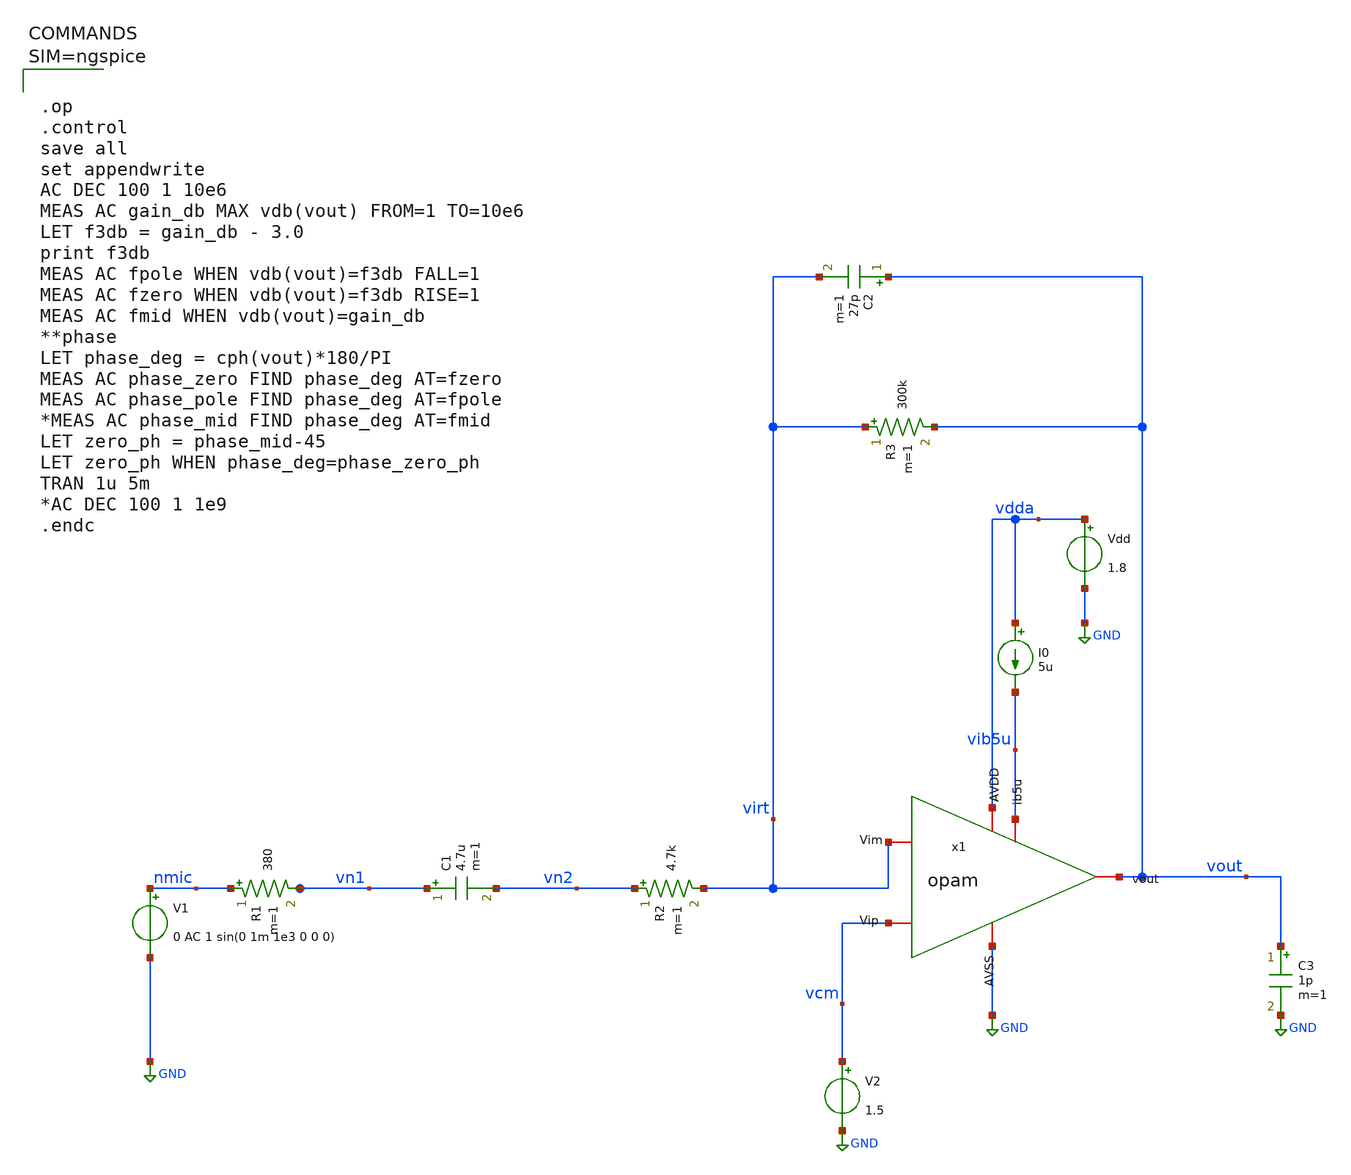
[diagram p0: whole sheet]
** sch_path: xschem/Main_opam_nmos.sch
**.subckt Main_opam_nmos
V1 nmic GND 0 AC 1 sin(0 1m 1e3 0 0 0)
R1 nmic vn1 380 m=1
C1 vn1 vn2 4.7u m=1
R2 vn2 virt 4.7k m=1
R3 virt vout 300k m=1
C2 vout virt 27p m=1
V2 vcm GND 1.5
C3 vout GND 1p m=1
x1 vdda vout virt vcm vib5u GND opam
I0 vdda vib5u 5u
Vdd vdda GND 1.8
**** begin user architecture code

** opencircuitdesign pdks install
.lib $::SKYWATER_MODELS/sky130.lib.spice tt




.op
.control
save all
set appendwrite
AC DEC 100 1 10e6
MEAS AC gain_db MAX vdb(vout) FROM=1 TO=10e6
LET f3db = gain_db - 3.0
print f3db
MEAS AC fpole WHEN vdb(vout)=f3db FALL=1
MEAS AC fzero WHEN vdb(vout)=f3db RISE=1
MEAS AC fmid WHEN vdb(vout)=gain_db
**phase
LET phase_deg = cph(vout)*180/PI
MEAS AC phase_zero FIND phase_deg AT=fzero
MEAS AC phase_pole FIND phase_deg AT=fpole
*MEAS AC phase_mid FIND phase_deg AT=fmid
LET zero_ph = phase_mid-45
LET zero_ph WHEN phase_deg=phase_zero_ph
TRAN 1u 5m
*AC DEC 100 1 1e9
.endc





**** end user architecture code
**.ends

* expanding   symbol:  opam.sym # of pins=6
** sym_path: xschem/opam.sym
** sch_path: xschem/opam.sch
.subckt opam AVDD vout Vim Vip ib5u AVSS
*.iopin AVSS
*.iopin ib5u
*.iopin AVDD
*.iopin Vip
*.iopin vout
*.iopin Vim
XMtail net1 ib5u AVSS AVSS sky130_fd_pr__nfet_01v8 L=1 W=5 nf=1 ad='int((1 + 1)/2) * 5 / 1 * 0.29' as='int((1 + 2)/2) * 5 / 1 * 0.29'
+ pd='2*int((1 + 1)/2) * (5 / 1 + 0.29)' ps='2*int((1 + 2)/2) * (5 / 1 + 0.29)' nrd='0.29 / 5 ' nrs='0.29 / 5 '
+ sa=0 sb=0 sd=0 mult=2 m=2
XM1 ib5u ib5u AVSS AVSS sky130_fd_pr__nfet_01v8 L=1 W=5 nf=1 ad='int((1 + 1)/2) * 5 / 1 * 0.29' as='int((1 + 2)/2) * 5 / 1 * 0.29'
+ pd='2*int((1 + 1)/2) * (5 / 1 + 0.29)' ps='2*int((1 + 2)/2) * (5 / 1 + 0.29)' nrd='0.29 / 5 ' nrs='0.29 / 5 '
+ sa=0 sb=0 sd=0 mult=1 m=1
XMip vom Vip net1 net1 sky130_fd_pr__nfet_01v8_lvt L=2 W=5 nf=1 ad='int((1 + 1)/2) * 5 / 1 * 0.29' as='int((1 + 2)/2) * 5 / 1 * 0.29'
+ pd='2*int((1 + 1)/2) * (5 / 1 + 0.29)' ps='2*int((1 + 2)/2) * (5 / 1 + 0.29)' nrd='0.29 / 5 ' nrs='0.29 / 5 '
+ sa=0 sb=0 sd=0 mult=4 m=4
XM4 vout Vim net1 net1 sky130_fd_pr__nfet_01v8_lvt L=2 W=5 nf=1 ad='int((1 + 1)/2) * 5 / 1 * 0.29' as='int((1 + 2)/2) * 5 / 1 * 0.29'
+ pd='2*int((1 + 1)/2) * (5 / 1 + 0.29)' ps='2*int((1 + 2)/2) * (5 / 1 + 0.29)' nrd='0.29 / 5 ' nrs='0.29 / 5 '
+ sa=0 sb=0 sd=0 mult=4 m=4
XMcp vom vom AVDD AVDD sky130_fd_pr__pfet_01v8_lvt L=2 W=5 nf=1 ad='int((1 + 1)/2) * 5 / 1 * 0.29' as='int((1 + 2)/2) * 5 / 1 * 0.29'
+ pd='2*int((1 + 1)/2) * (5 / 1 + 0.29)' ps='2*int((1 + 2)/2) * (5 / 1 + 0.29)' nrd='0.29 / 5 ' nrs='0.29 / 5 '
+ sa=0 sb=0 sd=0 mult=2 m=2
XMcm vout vom AVDD AVDD sky130_fd_pr__pfet_01v8_lvt L=2 W=5 nf=1 ad='int((1 + 1)/2) * 5 / 1 * 0.29' as='int((1 + 2)/2) * 5 / 1 * 0.29'
+ pd='2*int((1 + 1)/2) * (5 / 1 + 0.29)' ps='2*int((1 + 2)/2) * (5 / 1 + 0.29)' nrd='0.29 / 5 ' nrs='0.29 / 5 '
+ sa=0 sb=0 sd=0 mult=2 m=2
.ends

.GLOBAL GND
.end
